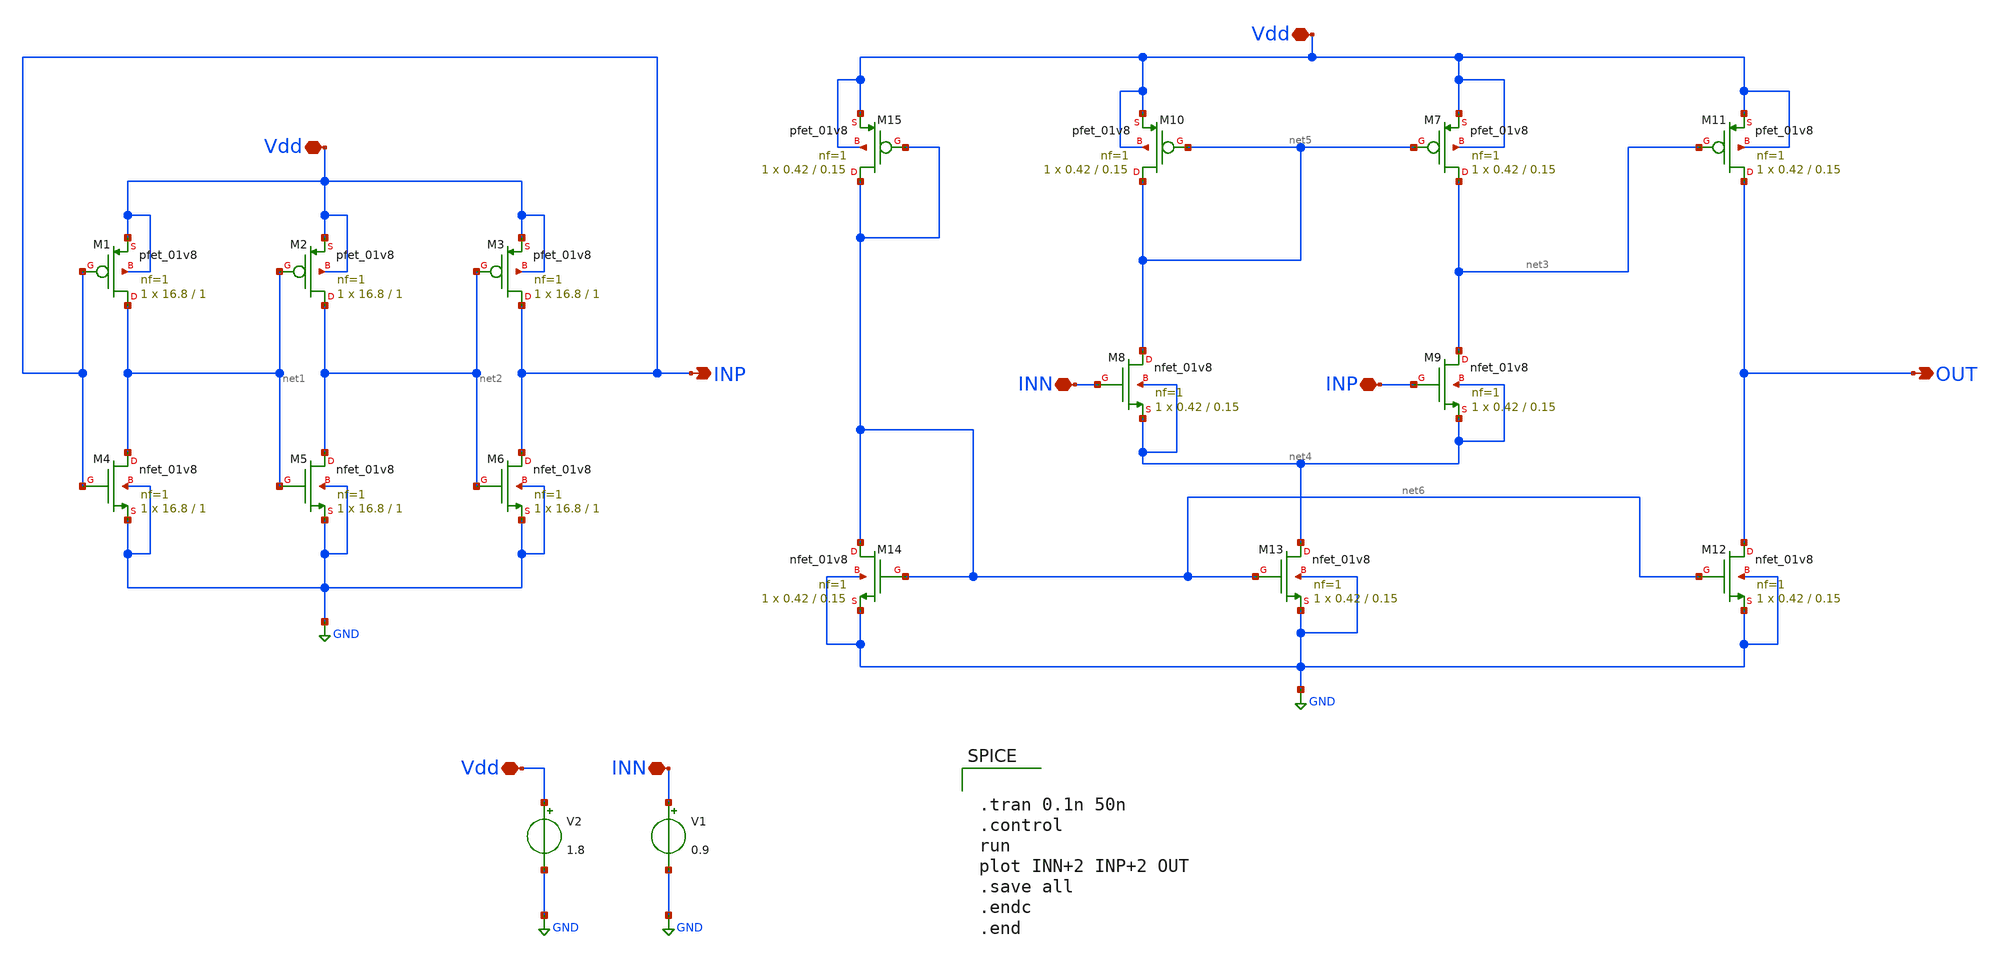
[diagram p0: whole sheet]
** sch_path: Week_4/RO_ADC_PreLayout/RO_ADC_pre.sch
**.subckt RO_ADC_pre INP Vdd INN INP OUT INN Vdd Vdd
*.opin INP
*.iopin Vdd
*.iopin INN
*.iopin INP
*.opin OUT
*.iopin INN
*.iopin Vdd
*.iopin Vdd
XM1 net1 INP Vdd Vdd sky130_fd_pr__pfet_01v8 L=1 W=16.8 nf=1 ad='int((nf+1)/2) * W/nf * 0.29' as='int((nf+2)/2) * W/nf * 0.29'
+ pd='2*int((nf+1)/2) * (W/nf + 0.29)' ps='2*int((nf+2)/2) * (W/nf + 0.29)' nrd='0.29 / W' nrs='0.29 / W'
+ sa=0 sb=0 sd=0 mult=1 m=1
XM2 net2 net1 Vdd Vdd sky130_fd_pr__pfet_01v8 L=1 W=16.8 nf=1 ad='int((nf+1)/2) * W/nf * 0.29' as='int((nf+2)/2) * W/nf * 0.29'
+ pd='2*int((nf+1)/2) * (W/nf + 0.29)' ps='2*int((nf+2)/2) * (W/nf + 0.29)' nrd='0.29 / W' nrs='0.29 / W'
+ sa=0 sb=0 sd=0 mult=1 m=1
XM3 INP net2 Vdd Vdd sky130_fd_pr__pfet_01v8 L=1 W=16.8 nf=1 ad='int((nf+1)/2) * W/nf * 0.29' as='int((nf+2)/2) * W/nf * 0.29'
+ pd='2*int((nf+1)/2) * (W/nf + 0.29)' ps='2*int((nf+2)/2) * (W/nf + 0.29)' nrd='0.29 / W' nrs='0.29 / W'
+ sa=0 sb=0 sd=0 mult=1 m=1
XM4 net1 INP GND GND sky130_fd_pr__nfet_01v8 L=1 W=16.8 nf=1 ad='int((nf+1)/2) * W/nf * 0.29' as='int((nf+2)/2) * W/nf * 0.29'
+ pd='2*int((nf+1)/2) * (W/nf + 0.29)' ps='2*int((nf+2)/2) * (W/nf + 0.29)' nrd='0.29 / W' nrs='0.29 / W'
+ sa=0 sb=0 sd=0 mult=1 m=1
XM5 net2 net1 GND GND sky130_fd_pr__nfet_01v8 L=1 W=16.8 nf=1 ad='int((nf+1)/2) * W/nf * 0.29' as='int((nf+2)/2) * W/nf * 0.29'
+ pd='2*int((nf+1)/2) * (W/nf + 0.29)' ps='2*int((nf+2)/2) * (W/nf + 0.29)' nrd='0.29 / W' nrs='0.29 / W'
+ sa=0 sb=0 sd=0 mult=1 m=1
XM6 INP net2 GND GND sky130_fd_pr__nfet_01v8 L=1 W=16.8 nf=1 ad='int((nf+1)/2) * W/nf * 0.29' as='int((nf+2)/2) * W/nf * 0.29'
+ pd='2*int((nf+1)/2) * (W/nf + 0.29)' ps='2*int((nf+2)/2) * (W/nf + 0.29)' nrd='0.29 / W' nrs='0.29 / W'
+ sa=0 sb=0 sd=0 mult=1 m=1
XM7 net3 net5 Vdd Vdd sky130_fd_pr__pfet_01v8 L=0.15 W=0.42 nf=1 ad='int((nf+1)/2) * W/nf * 0.29' as='int((nf+2)/2) * W/nf * 0.29'
+ pd='2*int((nf+1)/2) * (W/nf + 0.29)' ps='2*int((nf+2)/2) * (W/nf + 0.29)' nrd='0.29 / W' nrs='0.29 / W'
+ sa=0 sb=0 sd=0 mult=1 m=1
XM8 net5 INN net4 net4 sky130_fd_pr__nfet_01v8 L=0.15 W=0.42 nf=1 ad='int((nf+1)/2) * W/nf * 0.29' as='int((nf+2)/2) * W/nf * 0.29'
+ pd='2*int((nf+1)/2) * (W/nf + 0.29)' ps='2*int((nf+2)/2) * (W/nf + 0.29)' nrd='0.29 / W' nrs='0.29 / W'
+ sa=0 sb=0 sd=0 mult=1 m=1
XM9 net3 INP net4 net4 sky130_fd_pr__nfet_01v8 L=0.15 W=0.42 nf=1 ad='int((nf+1)/2) * W/nf * 0.29' as='int((nf+2)/2) * W/nf * 0.29'
+ pd='2*int((nf+1)/2) * (W/nf + 0.29)' ps='2*int((nf+2)/2) * (W/nf + 0.29)' nrd='0.29 / W' nrs='0.29 / W'
+ sa=0 sb=0 sd=0 mult=1 m=1
XM10 net5 net5 Vdd Vdd sky130_fd_pr__pfet_01v8 L=0.15 W=0.42 nf=1 ad='int((nf+1)/2) * W/nf * 0.29' as='int((nf+2)/2) * W/nf * 0.29'
+ pd='2*int((nf+1)/2) * (W/nf + 0.29)' ps='2*int((nf+2)/2) * (W/nf + 0.29)' nrd='0.29 / W' nrs='0.29 / W'
+ sa=0 sb=0 sd=0 mult=1 m=1
XM11 OUT net3 Vdd Vdd sky130_fd_pr__pfet_01v8 L=0.15 W=0.42 nf=1 ad='int((nf+1)/2) * W/nf * 0.29' as='int((nf+2)/2) * W/nf * 0.29'
+ pd='2*int((nf+1)/2) * (W/nf + 0.29)' ps='2*int((nf+2)/2) * (W/nf + 0.29)' nrd='0.29 / W' nrs='0.29 / W'
+ sa=0 sb=0 sd=0 mult=1 m=1
XM12 OUT net6 GND GND sky130_fd_pr__nfet_01v8 L=0.15 W=0.42 nf=1 ad='int((nf+1)/2) * W/nf * 0.29' as='int((nf+2)/2) * W/nf * 0.29'
+ pd='2*int((nf+1)/2) * (W/nf + 0.29)' ps='2*int((nf+2)/2) * (W/nf + 0.29)' nrd='0.29 / W' nrs='0.29 / W'
+ sa=0 sb=0 sd=0 mult=1 m=1
XM13 net4 net6 GND GND sky130_fd_pr__nfet_01v8 L=0.15 W=0.42 nf=1 ad='int((nf+1)/2) * W/nf * 0.29' as='int((nf+2)/2) * W/nf * 0.29'
+ pd='2*int((nf+1)/2) * (W/nf + 0.29)' ps='2*int((nf+2)/2) * (W/nf + 0.29)' nrd='0.29 / W' nrs='0.29 / W'
+ sa=0 sb=0 sd=0 mult=1 m=1
XM14 net6 net6 GND GND sky130_fd_pr__nfet_01v8 L=0.15 W=0.42 nf=1 ad='int((nf+1)/2) * W/nf * 0.29' as='int((nf+2)/2) * W/nf * 0.29'
+ pd='2*int((nf+1)/2) * (W/nf + 0.29)' ps='2*int((nf+2)/2) * (W/nf + 0.29)' nrd='0.29 / W' nrs='0.29 / W'
+ sa=0 sb=0 sd=0 mult=1 m=1
XM15 net6 net6 Vdd Vdd sky130_fd_pr__pfet_01v8 L=0.15 W=0.42 nf=1 ad='int((nf+1)/2) * W/nf * 0.29' as='int((nf+2)/2) * W/nf * 0.29'
+ pd='2*int((nf+1)/2) * (W/nf + 0.29)' ps='2*int((nf+2)/2) * (W/nf + 0.29)' nrd='0.29 / W' nrs='0.29 / W'
+ sa=0 sb=0 sd=0 mult=1 m=1
V1 INN GND 0.9
V2 Vdd GND 1.8
**** begin user architecture code


.lib /home/swagatika/open_pdks/sky130/sky130A/libs.tech/ngspice/sky130.lib.spice tt

.save all





.tran 0.1n 50n
.control
run
plot INN+2 INP+2 OUT
.save all
.endc
.end


**** end user architecture code
**.ends
.GLOBAL GND
.end
